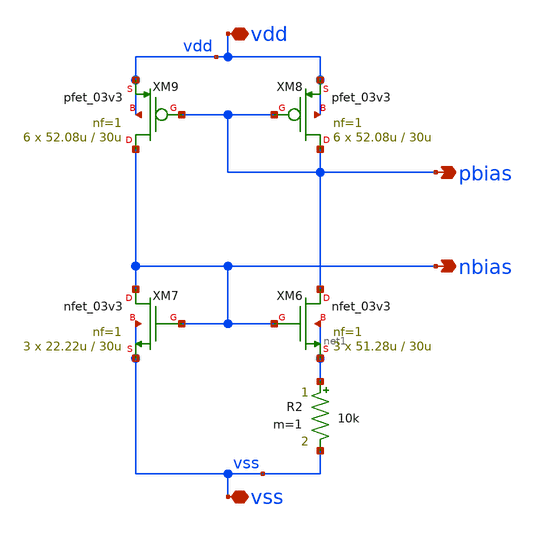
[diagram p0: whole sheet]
** sch_path: design/analog/beta multiplier/beta_multiplier.sch
**.subckt beta_multiplier vdd vss pbias nbias
*.iopin vdd
*.iopin vss
*.opin pbias
*.opin nbias
XM6 pbias nbias net1 net1 nfet_03v3 L=30u W=51.28u nf=1 ad='int((nf+1)/2) * W/nf * 0.18u' as='int((nf+2)/2) * W/nf * 0.18u'
+ pd='2*int((nf+1)/2) * (W/nf + 0.18u)' ps='2*int((nf+2)/2) * (W/nf + 0.18u)' nrd='0.18u / W' nrs='0.18u / W'
+ sa=0 sb=0 sd=0 m=3
XM7 nbias nbias vss vss nfet_03v3 L=30u W=22.22u nf=1 ad='int((nf+1)/2) * W/nf * 0.18u' as='int((nf+2)/2) * W/nf * 0.18u'
+ pd='2*int((nf+1)/2) * (W/nf + 0.18u)' ps='2*int((nf+2)/2) * (W/nf + 0.18u)' nrd='0.18u / W' nrs='0.18u / W'
+ sa=0 sb=0 sd=0 m=3
XM8 pbias pbias vdd vdd pfet_03v3 L=30u W=52.08u nf=1 ad='int((nf+1)/2) * W/nf * 0.18u' as='int((nf+2)/2) * W/nf * 0.18u'
+ pd='2*int((nf+1)/2) * (W/nf + 0.18u)' ps='2*int((nf+2)/2) * (W/nf + 0.18u)' nrd='0.18u / W' nrs='0.18u / W'
+ sa=0 sb=0 sd=0 m=6
XM9 nbias pbias vdd vdd pfet_03v3 L=30u W=52.08u nf=1 ad='int((nf+1)/2) * W/nf * 0.18u' as='int((nf+2)/2) * W/nf * 0.18u'
+ pd='2*int((nf+1)/2) * (W/nf + 0.18u)' ps='2*int((nf+2)/2) * (W/nf + 0.18u)' nrd='0.18u / W' nrs='0.18u / W'
+ sa=0 sb=0 sd=0 m=6
R2 net1 vss 10k m=1
**.ends
.end
